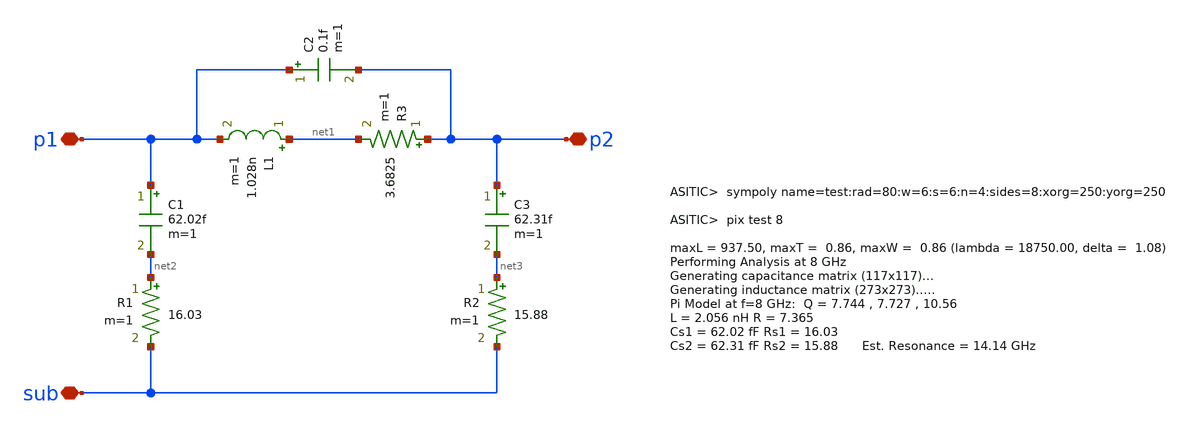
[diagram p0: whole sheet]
** sch_path: design/lc_oscillator_inductor/lc_oscillator_inductor.sch
**.subckt lc_oscillator_inductor p2 p1 sub
*.iopin p2
*.iopin p1
*.iopin sub
L1 net1 p1 1.028n m=1
C1 p1 net2 62.02f m=1
R1 net2 sub 16.03 m=1
C2 p1 p2 0.1f m=1
C3 p2 net3 62.31f m=1
R2 net3 sub 15.88 m=1
R3 p2 net1 3.6825 m=1
**.ends
.end
